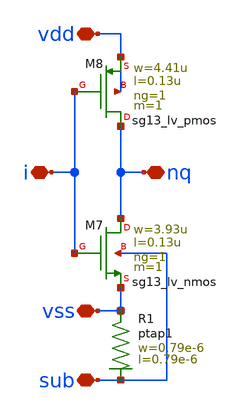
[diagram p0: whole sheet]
** sch_path: MSPHY6034-main/schematic/xschem/openpdk-libraries/ihp-sg13g2/sg13g2_io/xschem/sg13g2_io_inv_x1.sch
**.subckt sg13g2_io_inv_x1 vss nq i vdd sub
*.iopin vss
*.iopin nq
*.iopin i
*.iopin vdd
*.iopin sub
XR1 vss sub ptap1 R=259 w=0.79e-6 l=0.79e-6
XM7 nq i vss sub sg13_lv_nmos w=3.93u l=0.13u ng=1 m=1 mm_ok=1
XM8 nq i vdd vdd sg13_lv_pmos w=4.41u l=0.13u ng=1 m=1 mm_ok=1
**.ends
.end
